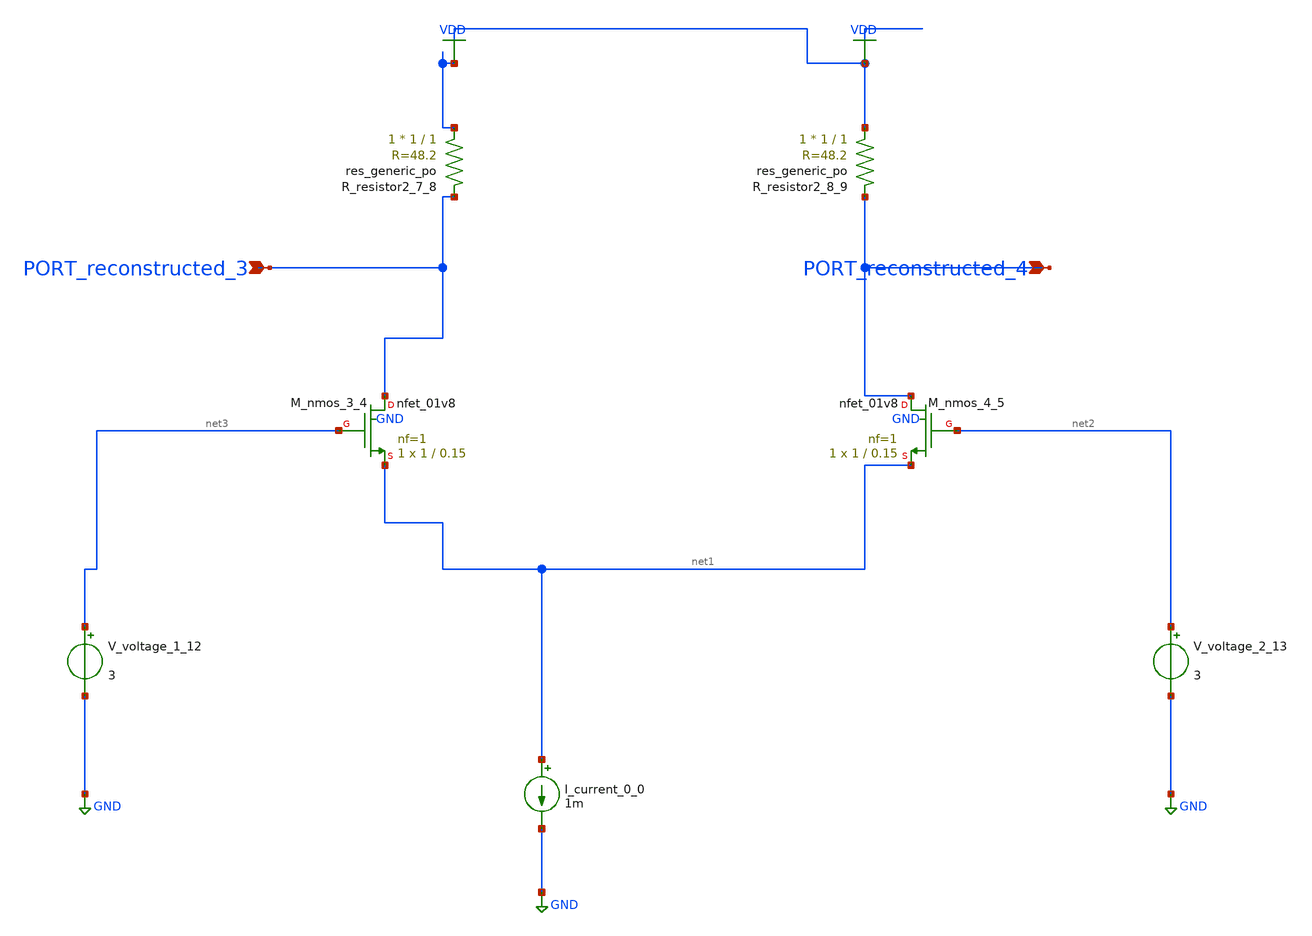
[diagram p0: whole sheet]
** sch_path: schematics/AMSNet/195.sch
**.subckt 195 PORT_reconstructed_3 PORT_reconstructed_4
*.ipin PORT_reconstructed_3
*.ipin PORT_reconstructed_4
I_current_0_0 net1 GND 1m
XM_nmos_3_4 PORT_reconstructed_3 net3 net1 GND sky130_fd_pr__nfet_01v8 L=0.15 W=1 nf=1 ad='int((1 + 1)/2) * 1 / 1 * 0.29'
+ as='int((1 + 2)/2) * 1 / 1 * 0.29' pd='2*int((1 + 1)/2) * (1 / 1 + 0.29)' ps='2*int((1 + 2)/2) * (1 / 1 + 0.29)'
+ nrd='0.29 / 1 ' nrs='0.29 / 1 ' sa=0 sb=0 sd=0 mult=1 m=1
XM_nmos_4_5 PORT_reconstructed_4 net2 net1 GND sky130_fd_pr__nfet_01v8 L=0.15 W=1 nf=1 ad='int((1 + 1)/2) * 1 / 1 * 0.29'
+ as='int((1 + 2)/2) * 1 / 1 * 0.29' pd='2*int((1 + 1)/2) * (1 / 1 + 0.29)' ps='2*int((1 + 2)/2) * (1 / 1 + 0.29)'
+ nrd='0.29 / 1 ' nrs='0.29 / 1 ' sa=0 sb=0 sd=0 mult=1 m=1
XR_resistor2_7_8 VDD PORT_reconstructed_3 sky130_fd_pr__res_generic_po W=1 L=1 m=1
XR_resistor2_8_9 VDD PORT_reconstructed_4 sky130_fd_pr__res_generic_po W=1 L=1 m=1
V_voltage_1_12 net3 GND 3
V_voltage_2_13 net2 GND 3
**.ends
.GLOBAL GND
.GLOBAL VDD
.end
